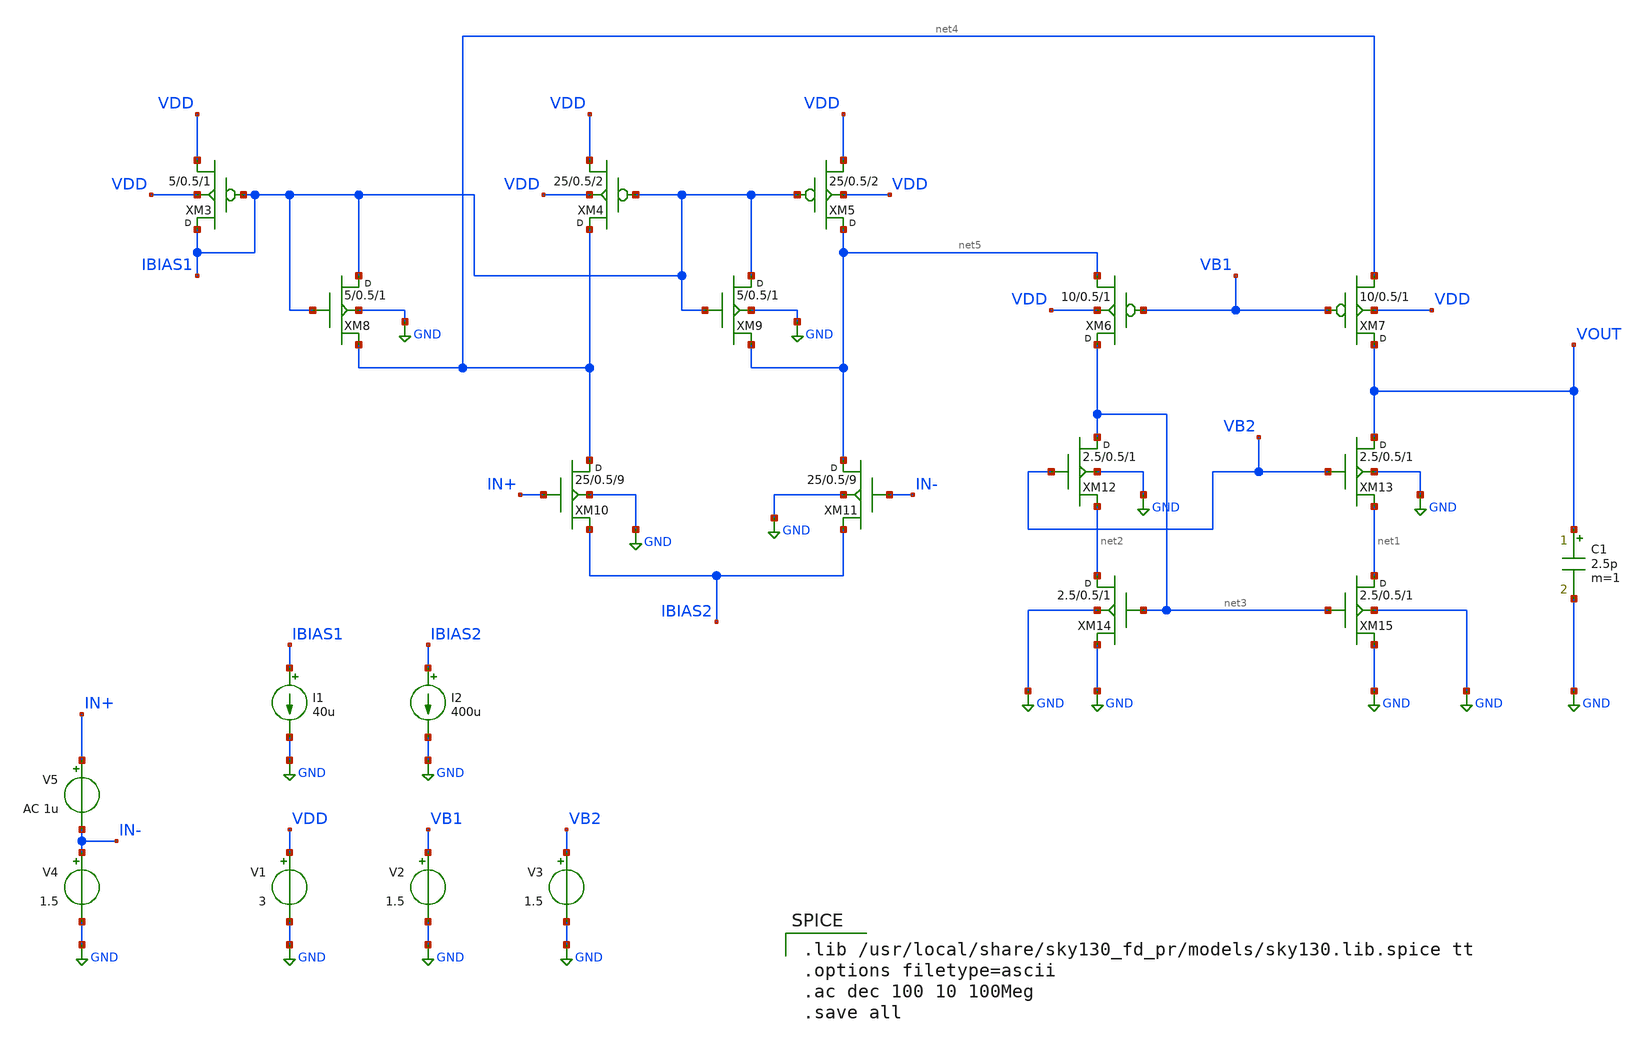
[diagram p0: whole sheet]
** sch_path: images/foss-asic-tools/addons/examples/sky130-analog/designs/basic_opa/basic_opamp.sch
**.subckt basic_opamp
XM3 IBIAS1 IBIAS1 VDD VDD sky130_fd_pr__pfet_g5v0d10v5 w=5 l=0.5 m=1
XM4 net4 IBIAS1 VDD VDD sky130_fd_pr__pfet_g5v0d10v5 w=25 l=0.5 m=2
XM5 net5 IBIAS1 VDD VDD sky130_fd_pr__pfet_g5v0d10v5 w=25 l=0.5 m=2
XM6 net3 VB1 net5 VDD sky130_fd_pr__pfet_g5v0d10v5 w=10 l=0.5 m=1
XM7 VOUT VB1 net4 VDD sky130_fd_pr__pfet_g5v0d10v5 w=10 l=0.5 m=1
XM8 IBIAS1 IBIAS1 net4 GND sky130_fd_pr__nfet_g5v0d10v5 w=5 l=0.5 m=1
XM9 IBIAS1 IBIAS1 net5 GND sky130_fd_pr__nfet_g5v0d10v5 w=5 l=0.5 m=1
XM10 net4 IN+ IBIAS2 GND sky130_fd_pr__nfet_g5v0d10v5 w=25 l=0.5 m=9
XM11 net5 IN- IBIAS2 GND sky130_fd_pr__nfet_g5v0d10v5 w=25 l=0.5 m=9
XM12 net3 VB2 net2 GND sky130_fd_pr__nfet_g5v0d10v5 w=2.5 l=0.5 m=1
XM13 VOUT VB2 net1 GND sky130_fd_pr__nfet_g5v0d10v5 w=2.5 l=0.5 m=1
XM14 net2 net3 GND GND sky130_fd_pr__nfet_g5v0d10v5 w=2.5 l=0.5 m=1
XM15 net1 net3 GND GND sky130_fd_pr__nfet_g5v0d10v5 w=2.5 l=0.5 m=1
I1 IBIAS1 GND 40u
I2 IBIAS2 GND 400u
V1 VDD GND 3
V2 VB1 GND 1.5
V3 VB2 GND 1.5
C1 VOUT GND 2.5p m=1
V4 IN- GND 1.5
V5 IN+ IN- AC 1u
**** begin user architecture code

.lib /usr/local/share/sky130_fd_pr/models/sky130.lib.spice tt
.options filetype=ascii
.ac dec 100 10 100Meg
.save all

**** end user architecture code
**.ends
.GLOBAL GND
.end
